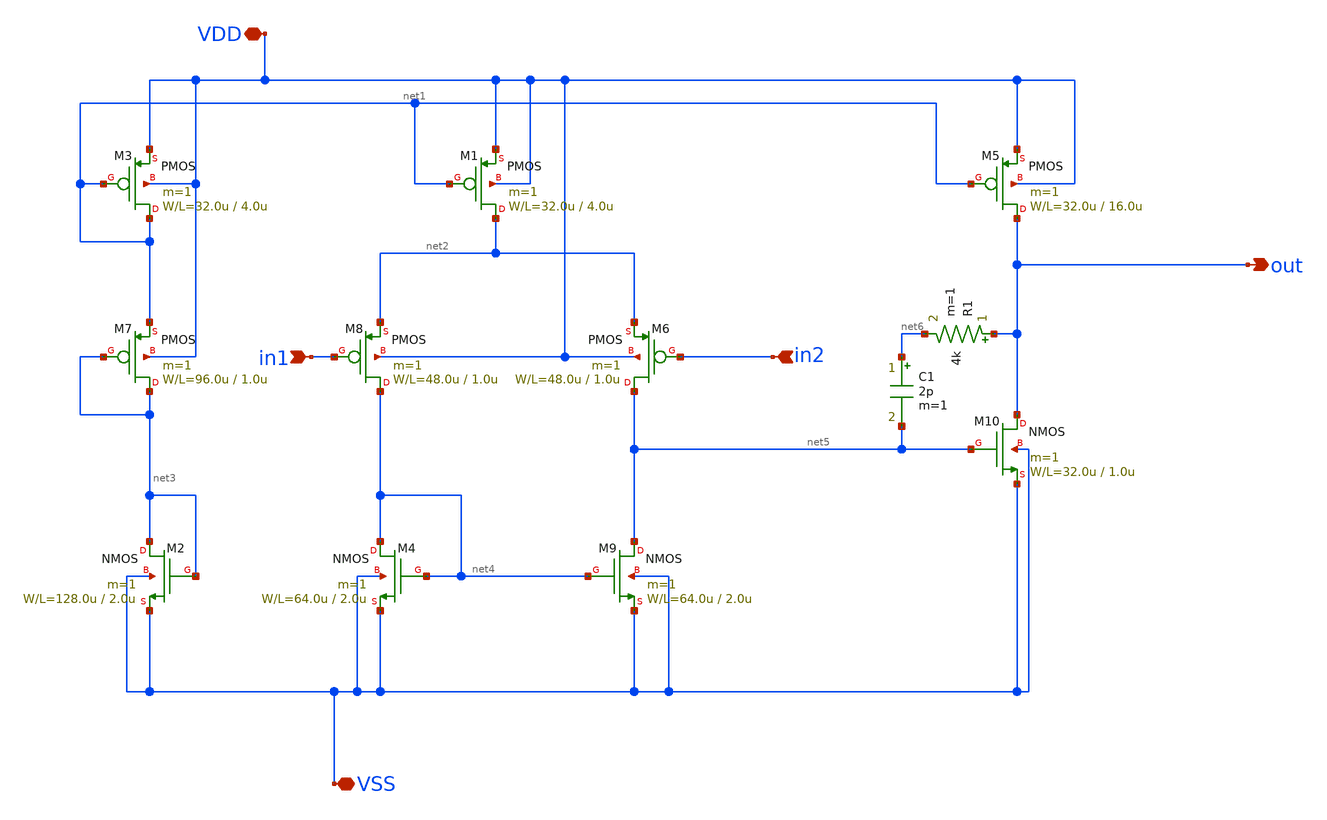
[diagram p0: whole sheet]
** sch_path: member_project/SaltyChip703/Op-amp1/opamp.sch
**.subckt opamp in1 out VDD VSS in2
*.ipin in1
*.opin out
*.iopin VDD
*.iopin VSS
*.ipin in2
M2 net3 net3 VSS VSS NMOS L=2.0u W=128.0u m=1
M1 net2 net1 VDD VDD PMOS L=4.0u W=32.0u m=1
M3 net1 net1 VDD VDD PMOS L=4.0u W=32.0u m=1
M4 net4 net4 VSS VSS NMOS L=2.0u W=64.0u m=1
M5 out net1 VDD VDD PMOS L=16.0u W=32.0u m=1
M6 net5 in2 net2 VDD PMOS L=1.0u W=48.0u m=1
M7 net3 net3 net1 VDD PMOS L=1.0u W=96.0u m=1
M8 net4 in1 net2 VDD PMOS L=1.0u W=48.0u m=1
M9 net5 net4 VSS VSS NMOS L=2.0u W=64.0u m=1
M10 out net5 VSS VSS NMOS L=1.0u W=32.0u m=1
R1 out net6 4k m=1
C1 net6 net5 2p m=1
**.ends
.end
